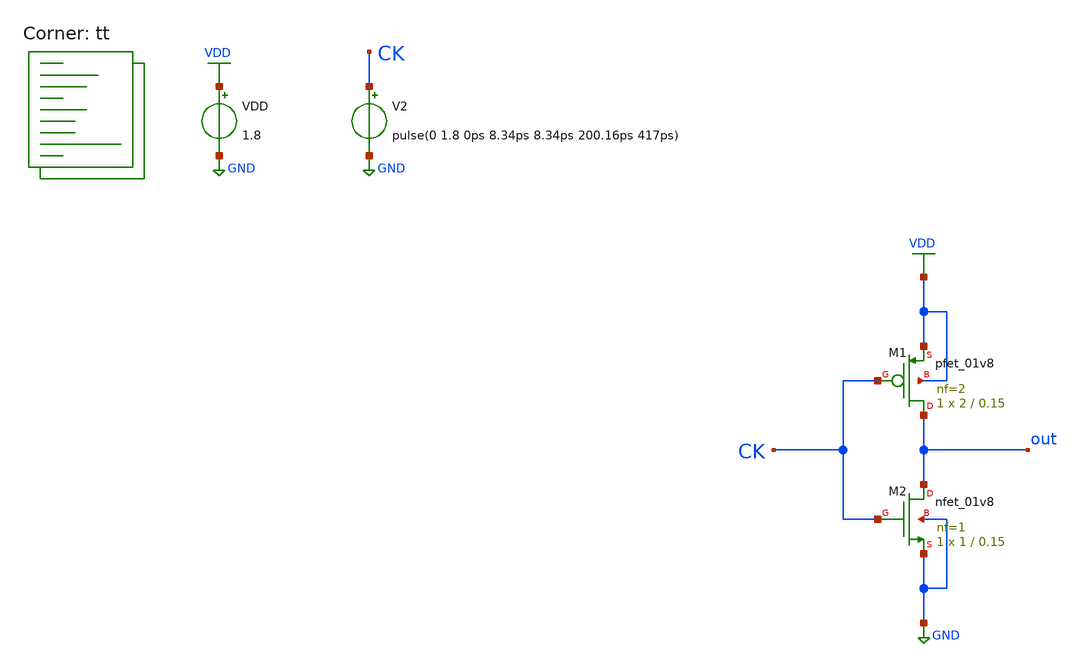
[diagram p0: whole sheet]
** sch_path: projects/pll/divider/xschem_ngspice/tb_TSPC_FF_comp_sw_divide3_8.sch
**.subckt tb_TSPC_FF_comp_sw_divide3_8
VDD VDD GND 1.8
V2 CK GND pulse(0 1.8 0ps 8.34ps 8.34ps 200.16ps 417ps)
XM1 out CK VDD VDD sky130_fd_pr__pfet_01v8 L=0.15 W=2 nf=2 ad='int((nf+1)/2) * W/nf * 0.29' as='int((nf+2)/2) * W/nf * 0.29'
+ pd='2*int((nf+1)/2) * (W/nf + 0.29)' ps='2*int((nf+2)/2) * (W/nf + 0.29)' nrd='0.29 / W' nrs='0.29 / W'
+ sa=0 sb=0 sd=0 mult=1 m=1
XM2 out CK GND GND sky130_fd_pr__nfet_01v8 L=0.15 W=1 nf=1 ad='int((nf+1)/2) * W/nf * 0.29' as='int((nf+2)/2) * W/nf * 0.29'
+ pd='2*int((nf+1)/2) * (W/nf + 0.29)' ps='2*int((nf+2)/2) * (W/nf + 0.29)' nrd='0.29 / W' nrs='0.29 / W'
+ sa=0 sb=0 sd=0 mult=1 m=1
**** begin user architecture code



.include /foss/pdks/sky130A/libs.ref/sky130_fd_sc_hd/spice/sky130_fd_sc_hd.spice

.option method=gear
.option wnflag=1
.option savecurrents

.save @m.xm1.msky130_fd_pr__pfet_01v8[gm] @m.xm2.msky130_fd_pr__nfet_01v8[gm]

.probe p(xm1) p(xm2)

.control

  save v(ck) v(out)
  * save all
  * tran 0.1n 1u
  tran 0.05p 20n

  remzerovec
  *linearize v(ck) v(d1) (q1) v(q1_b) v(q2_b) p(x1:power) p(x2:power) p(x3:power)
  write tb_TSPC_FF_comp_sw_divide3_8.raw
  * wrdata
+ /foss/designs/my_design/projects/pll/divider/xschem_ngspice/tb_TSPC_FF_comp_sw_divide3_7.txt p(x1:power) p(x2:power) p(x3:power)
  set appendwrite

.endc



.lib $::SKYWATER_MODELS/sky130.lib.spice tt
**** end user architecture code
**.ends
.GLOBAL GND
.GLOBAL VDD
.end
